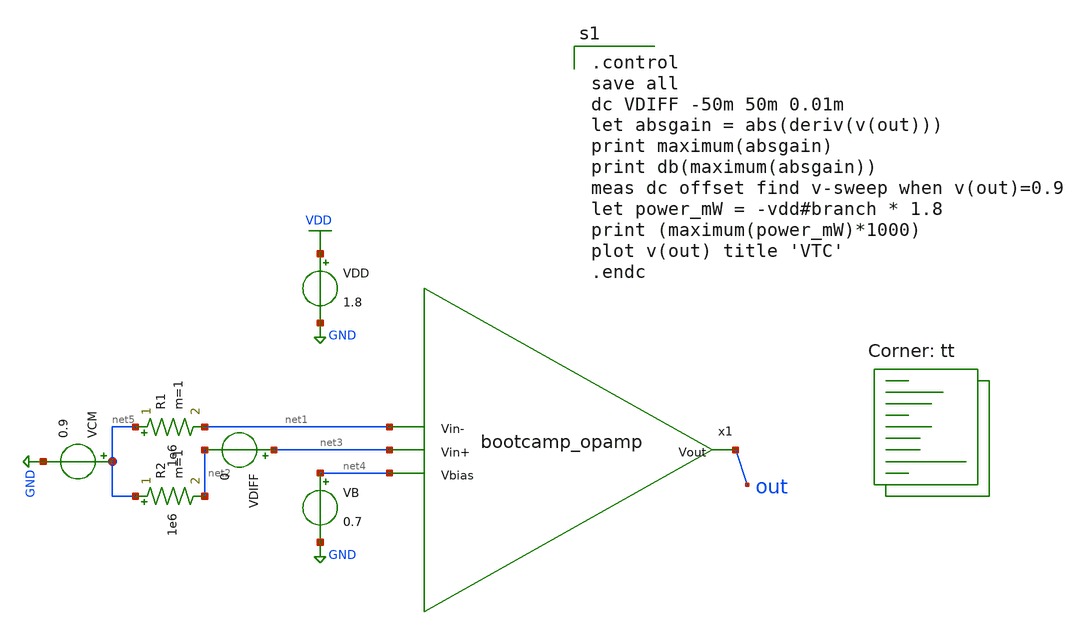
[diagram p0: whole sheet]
** sch_path: analog/schematics/tb_dc_analysis.sch
**.subckt tb_dc_analysis
x1 out net1 net3 net4 bootcamp_opamp
VDD VDD GND 1.8
VCM net5 GND 0.9
VB net4 GND 0.7
VDIFF net3 net2 0
R1 net5 net1 1e6 m=1
R2 net5 net2 1e6 m=1
**** begin user architecture code

.control
save all
dc VDIFF -50m 50m 0.01m
let absgain = abs(deriv(v(out)))
print maximum(absgain)
print db(maximum(absgain))
meas dc offset find v-sweep when v(out)=0.9
let power_mW = -vdd#branch * 1.8
print (maximum(power_mW)*1000)
plot v(out) title 'VTC'
.endc

.lib $::SKYWATER_MODELS/sky130.lib.spice tt
**** end user architecture code
**.ends
.GLOBAL GND
.GLOBAL VDD
.end
